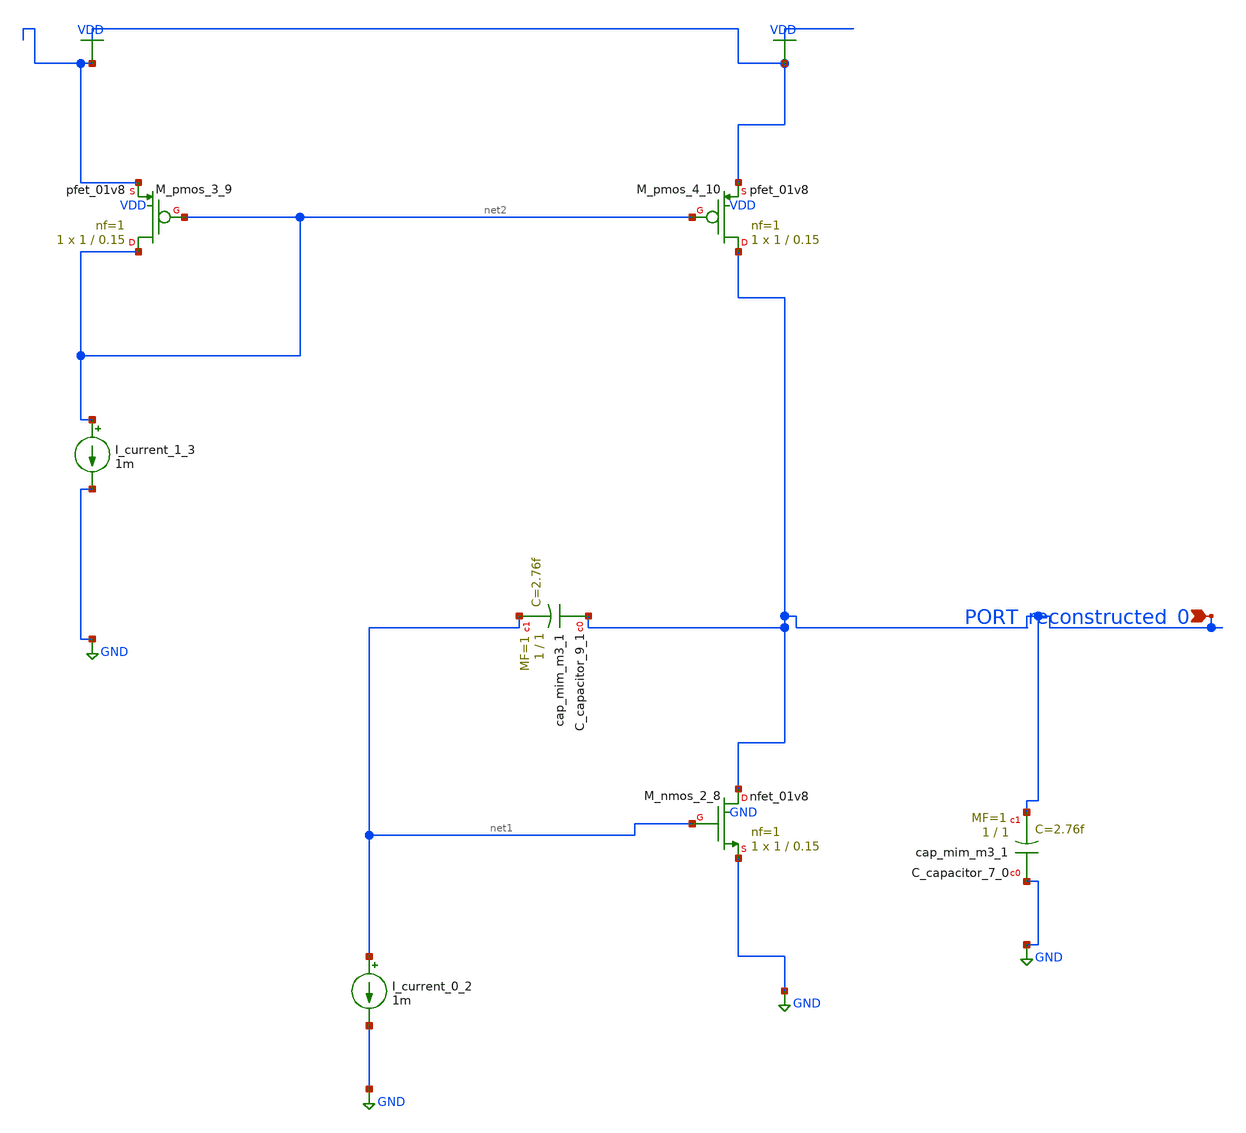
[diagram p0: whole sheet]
** sch_path: schematics/AMSNet/735.sch
**.subckt 735 PORT_reconstructed_0
*.ipin PORT_reconstructed_0
XC_capacitor_7_0 GND PORT_reconstructed_0 sky130_fd_pr__cap_mim_m3_1 W=1 L=1 MF=1 m=1
XC_capacitor_9_1 PORT_reconstructed_0 net1 sky130_fd_pr__cap_mim_m3_1 W=1 L=1 MF=1 m=1
I_current_0_2 net1 GND 1m
I_current_1_3 net2 GND 1m
XM_nmos_2_8 PORT_reconstructed_0 net1 GND GND sky130_fd_pr__nfet_01v8 L=0.15 W=1 nf=1 ad='int((1 + 1)/2) * 1 / 1 * 0.29'
+ as='int((1 + 2)/2) * 1 / 1 * 0.29' pd='2*int((1 + 1)/2) * (1 / 1 + 0.29)' ps='2*int((1 + 2)/2) * (1 / 1 + 0.29)'
+ nrd='0.29 / 1 ' nrs='0.29 / 1 ' sa=0 sb=0 sd=0 mult=1 m=1
XM_pmos_3_9 net2 net2 VDD VDD sky130_fd_pr__pfet_01v8 L=0.15 W=1 nf=1 ad='int((1 + 1)/2) * 1 / 1 * 0.29'
+ as='int((1 + 2)/2) * 1 / 1 * 0.29' pd='2*int((1 + 1)/2) * (1 / 1 + 0.29)' ps='2*int((1 + 2)/2) * (1 / 1 + 0.29)'
+ nrd='0.29 / 1 ' nrs='0.29 / 1 ' sa=0 sb=0 sd=0 mult=1 m=1
XM_pmos_4_10 PORT_reconstructed_0 net2 VDD VDD sky130_fd_pr__pfet_01v8 L=0.15 W=1 nf=1 ad='int((1 + 1)/2) * 1 / 1 * 0.29'
+ as='int((1 + 2)/2) * 1 / 1 * 0.29' pd='2*int((1 + 1)/2) * (1 / 1 + 0.29)' ps='2*int((1 + 2)/2) * (1 / 1 + 0.29)'
+ nrd='0.29 / 1 ' nrs='0.29 / 1 ' sa=0 sb=0 sd=0 mult=1 m=1
**.ends
.GLOBAL GND
.GLOBAL VDD
.end
